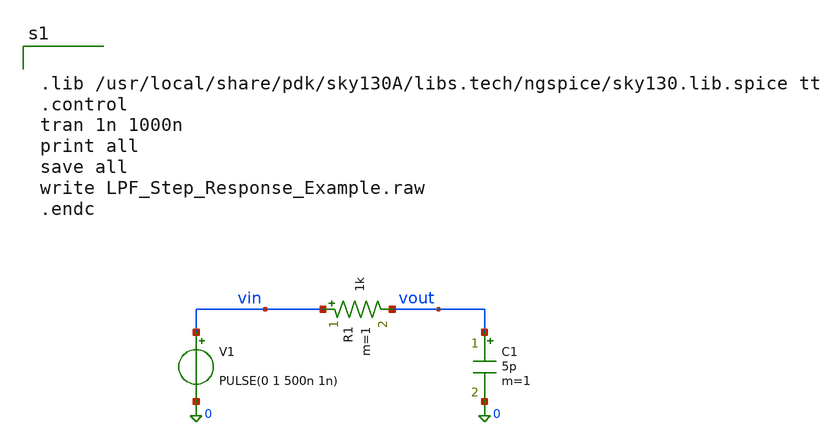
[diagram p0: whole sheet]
** sch_path: mag/LPF_Step_Response_Example.sch
**.subckt LPF_Step_Response_Example
V1 vin 0 PULSE(0 1 500n 1n)
R1 vin vout 1k m=1
C1 vout 0 5p m=1
**** begin user architecture code


.lib /usr/local/share/pdk/sky130A/libs.tech/ngspice/sky130.lib.spice tt
.control
tran 1n 1000n
print all
save all
write LPF_Step_Response_Example.raw
.endc

**** end user architecture code
**.ends
.end
